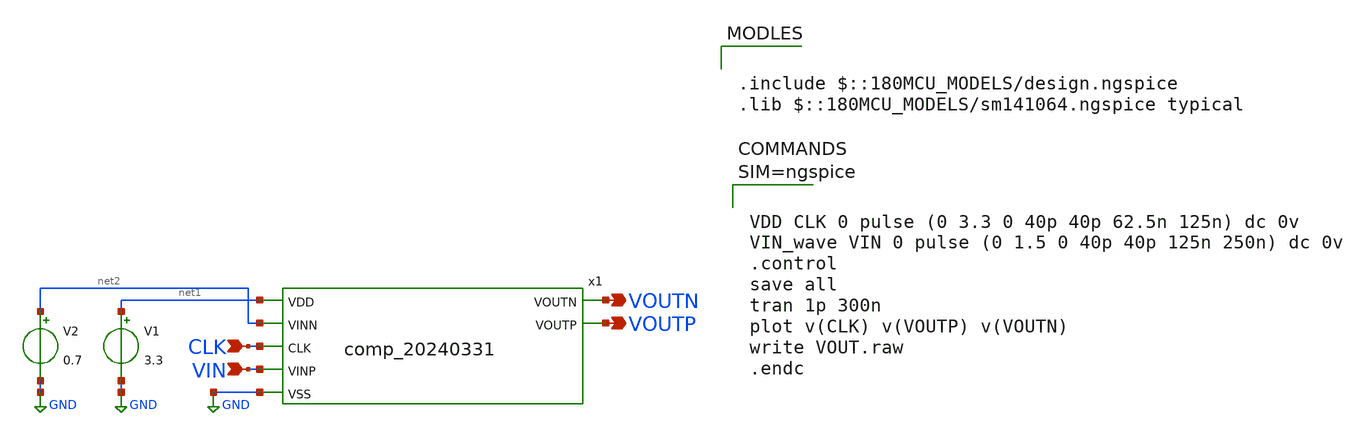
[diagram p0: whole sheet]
** sch_path: gitefu/tb/test_like_p78.sch
**.subckt test_like_p78 CLK VOUTN VOUTP VIN
*.ipin CLK
*.opin VOUTN
*.opin VOUTP
*.ipin VIN
V1 net1 GND 3.3
V2 net2 GND 0.7
x1 net1 net2 CLK VOUTN VOUTP VIN GND comp_20240331
**** begin user architecture code

.include $::180MCU_MODELS/design.ngspice
.lib $::180MCU_MODELS/sm141064.ngspice typical




VDD CLK 0 pulse (0 3.3 0 40p 40p 62.5n 125n) dc 0v
VIN_wave VIN 0 pulse (0 1.5 0 40p 40p 125n 250n) dc 0v
.control
save all
tran 1p 300n
plot v(CLK) v(VOUTP) v(VOUTN)
write VOUT.raw
.endc



**** end user architecture code
**.ends

* expanding   symbol:
*+  /media/tomoakitanaka/Documents/MyDocuments/personal/ISHIKAI/2024/Chipathon2023_ADC/gitefu/comp_20240331/comp_20240331.sym # of pins=7
** sym_path: gitefu/comp_20240331/comp_20240331.sym
** sch_path: gitefu/comp_20240331/comp_20240331.sch
.subckt comp_20240331 VDD VINN CLK VOUTN VOUTP VINP VSS
*.ipin VDD
*.ipin CLK
*.ipin VINP
*.ipin VINN
*.ipin VSS
*.opin VOUTP
*.opin VOUTN
XM1 net3 CLK VSS VSS nfet_03v3 L=0.28u W=2.80u nf=1 ad='int((nf+1)/2) * W/nf * 0.18u' as='int((nf+2)/2) * W/nf * 0.18u'
+ pd='2*int((nf+1)/2) * (W/nf + 0.18u)' ps='2*int((nf+2)/2) * (W/nf + 0.18u)' nrd='0.18u / W' nrs='0.18u / W'
+ sa=0 sb=0 sd=0 m=1
XM2 net1 VINP net3 VSS nfet_03v3 L=0.28u W=2.80u nf=1 ad='int((nf+1)/2) * W/nf * 0.18u' as='int((nf+2)/2) * W/nf * 0.18u'
+ pd='2*int((nf+1)/2) * (W/nf + 0.18u)' ps='2*int((nf+2)/2) * (W/nf + 0.18u)' nrd='0.18u / W' nrs='0.18u / W'
+ sa=0 sb=0 sd=0 m=1
XM4 net1 CLK VDD VDD pfet_03v3 L=0.28u W=2.80u nf=1 ad='int((nf+1)/2) * W/nf * 0.18u' as='int((nf+2)/2) * W/nf * 0.18u'
+ pd='2*int((nf+1)/2) * (W/nf + 0.18u)' ps='2*int((nf+2)/2) * (W/nf + 0.18u)' nrd='0.18u / W' nrs='0.18u / W'
+ sa=0 sb=0 sd=0 m=1
XM6 net4 net1 VDD VDD pfet_03v3 L=0.28u W=2.80u nf=1 ad='int((nf+1)/2) * W/nf * 0.18u' as='int((nf+2)/2) * W/nf * 0.18u'
+ pd='2*int((nf+1)/2) * (W/nf + 0.18u)' ps='2*int((nf+2)/2) * (W/nf + 0.18u)' nrd='0.18u / W' nrs='0.18u / W'
+ sa=0 sb=0 sd=0 m=1
XM7 VOUTP VOUTN net4 VDD pfet_03v3 L=0.28u W=2.80u nf=1 ad='int((nf+1)/2) * W/nf * 0.18u' as='int((nf+2)/2) * W/nf * 0.18u'
+ pd='2*int((nf+1)/2) * (W/nf + 0.18u)' ps='2*int((nf+2)/2) * (W/nf + 0.18u)' nrd='0.18u / W' nrs='0.18u / W'
+ sa=0 sb=0 sd=0 m=1
XM8 net4 net1 VSS VSS nfet_03v3 L=0.28u W=2.80u nf=1 ad='int((nf+1)/2) * W/nf * 0.18u' as='int((nf+2)/2) * W/nf * 0.18u'
+ pd='2*int((nf+1)/2) * (W/nf + 0.18u)' ps='2*int((nf+2)/2) * (W/nf + 0.18u)' nrd='0.18u / W' nrs='0.18u / W'
+ sa=0 sb=0 sd=0 m=1
XM9 VOUTP net1 VSS VSS nfet_03v3 L=0.28u W=2.80u nf=1 ad='int((nf+1)/2) * W/nf * 0.18u' as='int((nf+2)/2) * W/nf * 0.18u'
+ pd='2*int((nf+1)/2) * (W/nf + 0.18u)' ps='2*int((nf+2)/2) * (W/nf + 0.18u)' nrd='0.18u / W' nrs='0.18u / W'
+ sa=0 sb=0 sd=0 m=1
XM10 VOUTP VOUTN VSS VSS nfet_03v3 L=0.28u W=2.80u nf=1 ad='int((nf+1)/2) * W/nf * 0.18u' as='int((nf+2)/2) * W/nf * 0.18u'
+ pd='2*int((nf+1)/2) * (W/nf + 0.18u)' ps='2*int((nf+2)/2) * (W/nf + 0.18u)' nrd='0.18u / W' nrs='0.18u / W'
+ sa=0 sb=0 sd=0 m=1
XM3 net2 VINN net3 VSS nfet_03v3 L=0.28u W=2.80u nf=1 ad='int((nf+1)/2) * W/nf * 0.18u' as='int((nf+2)/2) * W/nf * 0.18u'
+ pd='2*int((nf+1)/2) * (W/nf + 0.18u)' ps='2*int((nf+2)/2) * (W/nf + 0.18u)' nrd='0.18u / W' nrs='0.18u / W'
+ sa=0 sb=0 sd=0 m=1
XM5 net2 CLK VDD VDD pfet_03v3 L=0.28u W=2.80u nf=1 ad='int((nf+1)/2) * W/nf * 0.18u' as='int((nf+2)/2) * W/nf * 0.18u'
+ pd='2*int((nf+1)/2) * (W/nf + 0.18u)' ps='2*int((nf+2)/2) * (W/nf + 0.18u)' nrd='0.18u / W' nrs='0.18u / W'
+ sa=0 sb=0 sd=0 m=1
XM11 net5 net2 VDD VDD pfet_03v3 L=0.28u W=2.80u nf=1 ad='int((nf+1)/2) * W/nf * 0.18u' as='int((nf+2)/2) * W/nf * 0.18u'
+ pd='2*int((nf+1)/2) * (W/nf + 0.18u)' ps='2*int((nf+2)/2) * (W/nf + 0.18u)' nrd='0.18u / W' nrs='0.18u / W'
+ sa=0 sb=0 sd=0 m=1
XM12 VOUTN VOUTP net5 VDD pfet_03v3 L=0.28u W=2.80u nf=1 ad='int((nf+1)/2) * W/nf * 0.18u' as='int((nf+2)/2) * W/nf * 0.18u'
+ pd='2*int((nf+1)/2) * (W/nf + 0.18u)' ps='2*int((nf+2)/2) * (W/nf + 0.18u)' nrd='0.18u / W' nrs='0.18u / W'
+ sa=0 sb=0 sd=0 m=1
XM13 net5 net2 VSS VSS nfet_03v3 L=0.28u W=2.80u nf=1 ad='int((nf+1)/2) * W/nf * 0.18u' as='int((nf+2)/2) * W/nf * 0.18u'
+ pd='2*int((nf+1)/2) * (W/nf + 0.18u)' ps='2*int((nf+2)/2) * (W/nf + 0.18u)' nrd='0.18u / W' nrs='0.18u / W'
+ sa=0 sb=0 sd=0 m=1
XM14 VOUTN net2 VSS VSS nfet_03v3 L=0.28u W=2.80u nf=1 ad='int((nf+1)/2) * W/nf * 0.18u' as='int((nf+2)/2) * W/nf * 0.18u'
+ pd='2*int((nf+1)/2) * (W/nf + 0.18u)' ps='2*int((nf+2)/2) * (W/nf + 0.18u)' nrd='0.18u / W' nrs='0.18u / W'
+ sa=0 sb=0 sd=0 m=1
XM15 VOUTN VOUTP VSS VSS nfet_03v3 L=0.28u W=2.80u nf=1 ad='int((nf+1)/2) * W/nf * 0.18u' as='int((nf+2)/2) * W/nf * 0.18u'
+ pd='2*int((nf+1)/2) * (W/nf + 0.18u)' ps='2*int((nf+2)/2) * (W/nf + 0.18u)' nrd='0.18u / W' nrs='0.18u / W'
+ sa=0 sb=0 sd=0 m=1
.ends

.GLOBAL GND
.end
